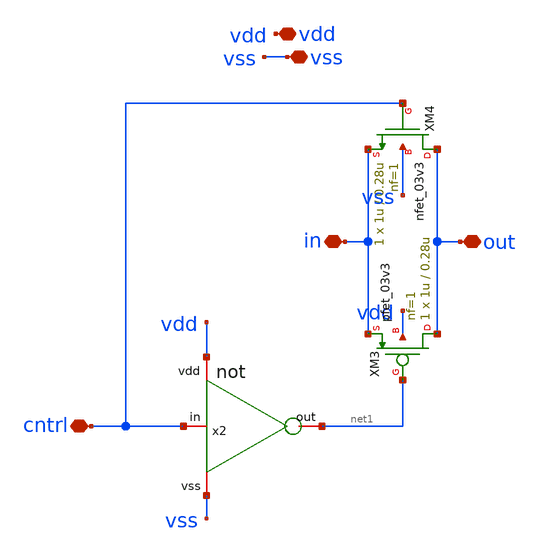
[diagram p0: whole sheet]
** sch_path: designs/tswitch_tb.sch
**.subckt tswitch_tb vdd vss in out cntrl
*.iopin vdd
*.iopin vss
*.iopin in
*.iopin out
*.iopin cntrl
XM3 out net1 in vdd pfet_03v3 L=0.28u W=1u nf=1 ad='int((nf+1)/2) * W/nf * 0.18u' as='int((nf+2)/2) * W/nf * 0.18u'
+ pd='2*int((nf+1)/2) * (W/nf + 0.18u)' ps='2*int((nf+2)/2) * (W/nf + 0.18u)' nrd='0.18u / W' nrs='0.18u / W'
+ sa=0 sb=0 sd=0 m=1
XM4 out cntrl in vss nfet_03v3 L=0.28u W=1u nf=1 ad='int((nf+1)/2) * W/nf * 0.18u' as='int((nf+2)/2) * W/nf * 0.18u'
+ pd='2*int((nf+1)/2) * (W/nf + 0.18u)' ps='2*int((nf+2)/2) * (W/nf + 0.18u)' nrd='0.18u / W' nrs='0.18u / W'
+ sa=0 sb=0 sd=0 m=1
x2 vdd cntrl net1 vss not
**.ends
.end
